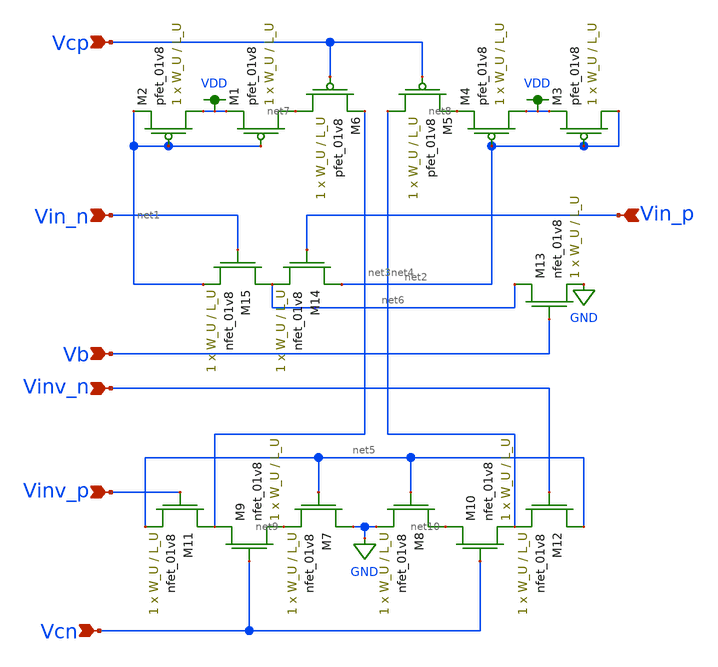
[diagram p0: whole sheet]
** sch_path: schematics/ota_lds.sch
**.subckt ota_lds Vcp Vcn Vinv_p Vinv_n Vb Vin_n Vin_p
*.ipin Vcp
*.ipin Vcn
*.ipin Vinv_p
*.ipin Vinv_n
*.ipin Vb
*.ipin Vin_n
*.ipin Vin_p
XM1 net7 net1 VDD VDD sky130_fd_pr__pfet_01v8 L=L_U W=W_U nf=1 ad='int((nf+1)/2) * W/nf * 0.29' as='int((nf+2)/2) * W/nf * 0.29'
+ pd='2*int((nf+1)/2) * (W/nf + 0.29)' ps='2*int((nf+2)/2) * (W/nf + 0.29)' nrd='0.29 / W' nrs='0.29 / W'
+ sa=0 sb=0 sd=0 mult=1 m=1
XM2 VDD net1 net1 VDD sky130_fd_pr__pfet_01v8 L=L_U W=W_U nf=1 ad='int((nf+1)/2) * W/nf * 0.29' as='int((nf+2)/2) * W/nf * 0.29'
+ pd='2*int((nf+1)/2) * (W/nf + 0.29)' ps='2*int((nf+2)/2) * (W/nf + 0.29)' nrd='0.29 / W' nrs='0.29 / W'
+ sa=0 sb=0 sd=0 mult=1 m=1
XM3 net2 net2 VDD VDD sky130_fd_pr__pfet_01v8 L=L_U W=W_U nf=1 ad='int((nf+1)/2) * W/nf * 0.29' as='int((nf+2)/2) * W/nf * 0.29'
+ pd='2*int((nf+1)/2) * (W/nf + 0.29)' ps='2*int((nf+2)/2) * (W/nf + 0.29)' nrd='0.29 / W' nrs='0.29 / W'
+ sa=0 sb=0 sd=0 mult=1 m=1
XM4 VDD net2 net8 VDD sky130_fd_pr__pfet_01v8 L=L_U W=W_U nf=1 ad='int((nf+1)/2) * W/nf * 0.29' as='int((nf+2)/2) * W/nf * 0.29'
+ pd='2*int((nf+1)/2) * (W/nf + 0.29)' ps='2*int((nf+2)/2) * (W/nf + 0.29)' nrd='0.29 / W' nrs='0.29 / W'
+ sa=0 sb=0 sd=0 mult=1 m=1
XM5 net4 Vcp net8 VDD sky130_fd_pr__pfet_01v8 L=L_U W=W_U nf=1 ad='int((nf+1)/2) * W/nf * 0.29' as='int((nf+2)/2) * W/nf * 0.29'
+ pd='2*int((nf+1)/2) * (W/nf + 0.29)' ps='2*int((nf+2)/2) * (W/nf + 0.29)' nrd='0.29 / W' nrs='0.29 / W'
+ sa=0 sb=0 sd=0 mult=1 m=1
XM6 net7 Vcp net3 VDD sky130_fd_pr__pfet_01v8 L=L_U W=W_U nf=1 ad='int((nf+1)/2) * W/nf * 0.29' as='int((nf+2)/2) * W/nf * 0.29'
+ pd='2*int((nf+1)/2) * (W/nf + 0.29)' ps='2*int((nf+2)/2) * (W/nf + 0.29)' nrd='0.29 / W' nrs='0.29 / W'
+ sa=0 sb=0 sd=0 mult=1 m=1
XM7 GND net5 net9 GND sky130_fd_pr__nfet_01v8 L=L_U W=W_U nf=1 ad='int((nf+1)/2) * W/nf * 0.29' as='int((nf+2)/2) * W/nf * 0.29'
+ pd='2*int((nf+1)/2) * (W/nf + 0.29)' ps='2*int((nf+2)/2) * (W/nf + 0.29)' nrd='0.29 / W' nrs='0.29 / W'
+ sa=0 sb=0 sd=0 mult=1 m=1
XM8 net10 net5 GND GND sky130_fd_pr__nfet_01v8 L=L_U W=W_U nf=1 ad='int((nf+1)/2) * W/nf * 0.29' as='int((nf+2)/2) * W/nf * 0.29'
+ pd='2*int((nf+1)/2) * (W/nf + 0.29)' ps='2*int((nf+2)/2) * (W/nf + 0.29)' nrd='0.29 / W' nrs='0.29 / W'
+ sa=0 sb=0 sd=0 mult=1 m=1
XM9 net3 Vcn net9 GND sky130_fd_pr__nfet_01v8 L=L_U W=W_U nf=1 ad='int((nf+1)/2) * W/nf * 0.29' as='int((nf+2)/2) * W/nf * 0.29'
+ pd='2*int((nf+1)/2) * (W/nf + 0.29)' ps='2*int((nf+2)/2) * (W/nf + 0.29)' nrd='0.29 / W' nrs='0.29 / W'
+ sa=0 sb=0 sd=0 mult=1 m=1
XM10 net10 Vcn net4 GND sky130_fd_pr__nfet_01v8 L=L_U W=W_U nf=1 ad='int((nf+1)/2) * W/nf * 0.29' as='int((nf+2)/2) * W/nf * 0.29'
+ pd='2*int((nf+1)/2) * (W/nf + 0.29)' ps='2*int((nf+2)/2) * (W/nf + 0.29)' nrd='0.29 / W' nrs='0.29 / W'
+ sa=0 sb=0 sd=0 mult=1 m=1
XM11 net3 Vinv_p net5 GND sky130_fd_pr__nfet_01v8 L=L_U W=W_U nf=1 ad='int((nf+1)/2) * W/nf * 0.29' as='int((nf+2)/2) * W/nf * 0.29'
+ pd='2*int((nf+1)/2) * (W/nf + 0.29)' ps='2*int((nf+2)/2) * (W/nf + 0.29)' nrd='0.29 / W' nrs='0.29 / W'
+ sa=0 sb=0 sd=0 mult=1 m=1
XM12 net5 Vinv_n net4 GND sky130_fd_pr__nfet_01v8 L=L_U W=W_U nf=1 ad='int((nf+1)/2) * W/nf * 0.29' as='int((nf+2)/2) * W/nf * 0.29'
+ pd='2*int((nf+1)/2) * (W/nf + 0.29)' ps='2*int((nf+2)/2) * (W/nf + 0.29)' nrd='0.29 / W' nrs='0.29 / W'
+ sa=0 sb=0 sd=0 mult=1 m=1
XM13 net6 Vb GND GND sky130_fd_pr__nfet_01v8 L=L_U W=W_U nf=1 ad='int((nf+1)/2) * W/nf * 0.29' as='int((nf+2)/2) * W/nf * 0.29'
+ pd='2*int((nf+1)/2) * (W/nf + 0.29)' ps='2*int((nf+2)/2) * (W/nf + 0.29)' nrd='0.29 / W' nrs='0.29 / W'
+ sa=0 sb=0 sd=0 mult=1 m=1
XM14 net2 Vin_p net6 GND sky130_fd_pr__nfet_01v8 L=L_U W=W_U nf=1 ad='int((nf+1)/2) * W/nf * 0.29' as='int((nf+2)/2) * W/nf * 0.29'
+ pd='2*int((nf+1)/2) * (W/nf + 0.29)' ps='2*int((nf+2)/2) * (W/nf + 0.29)' nrd='0.29 / W' nrs='0.29 / W'
+ sa=0 sb=0 sd=0 mult=1 m=1
XM15 net6 Vin_n net1 GND sky130_fd_pr__nfet_01v8 L=L_U W=W_U nf=1 ad='int((nf+1)/2) * W/nf * 0.29' as='int((nf+2)/2) * W/nf * 0.29'
+ pd='2*int((nf+1)/2) * (W/nf + 0.29)' ps='2*int((nf+2)/2) * (W/nf + 0.29)' nrd='0.29 / W' nrs='0.29 / W'
+ sa=0 sb=0 sd=0 mult=1 m=1
**.ends
.GLOBAL VDD
.GLOBAL GND
.end
